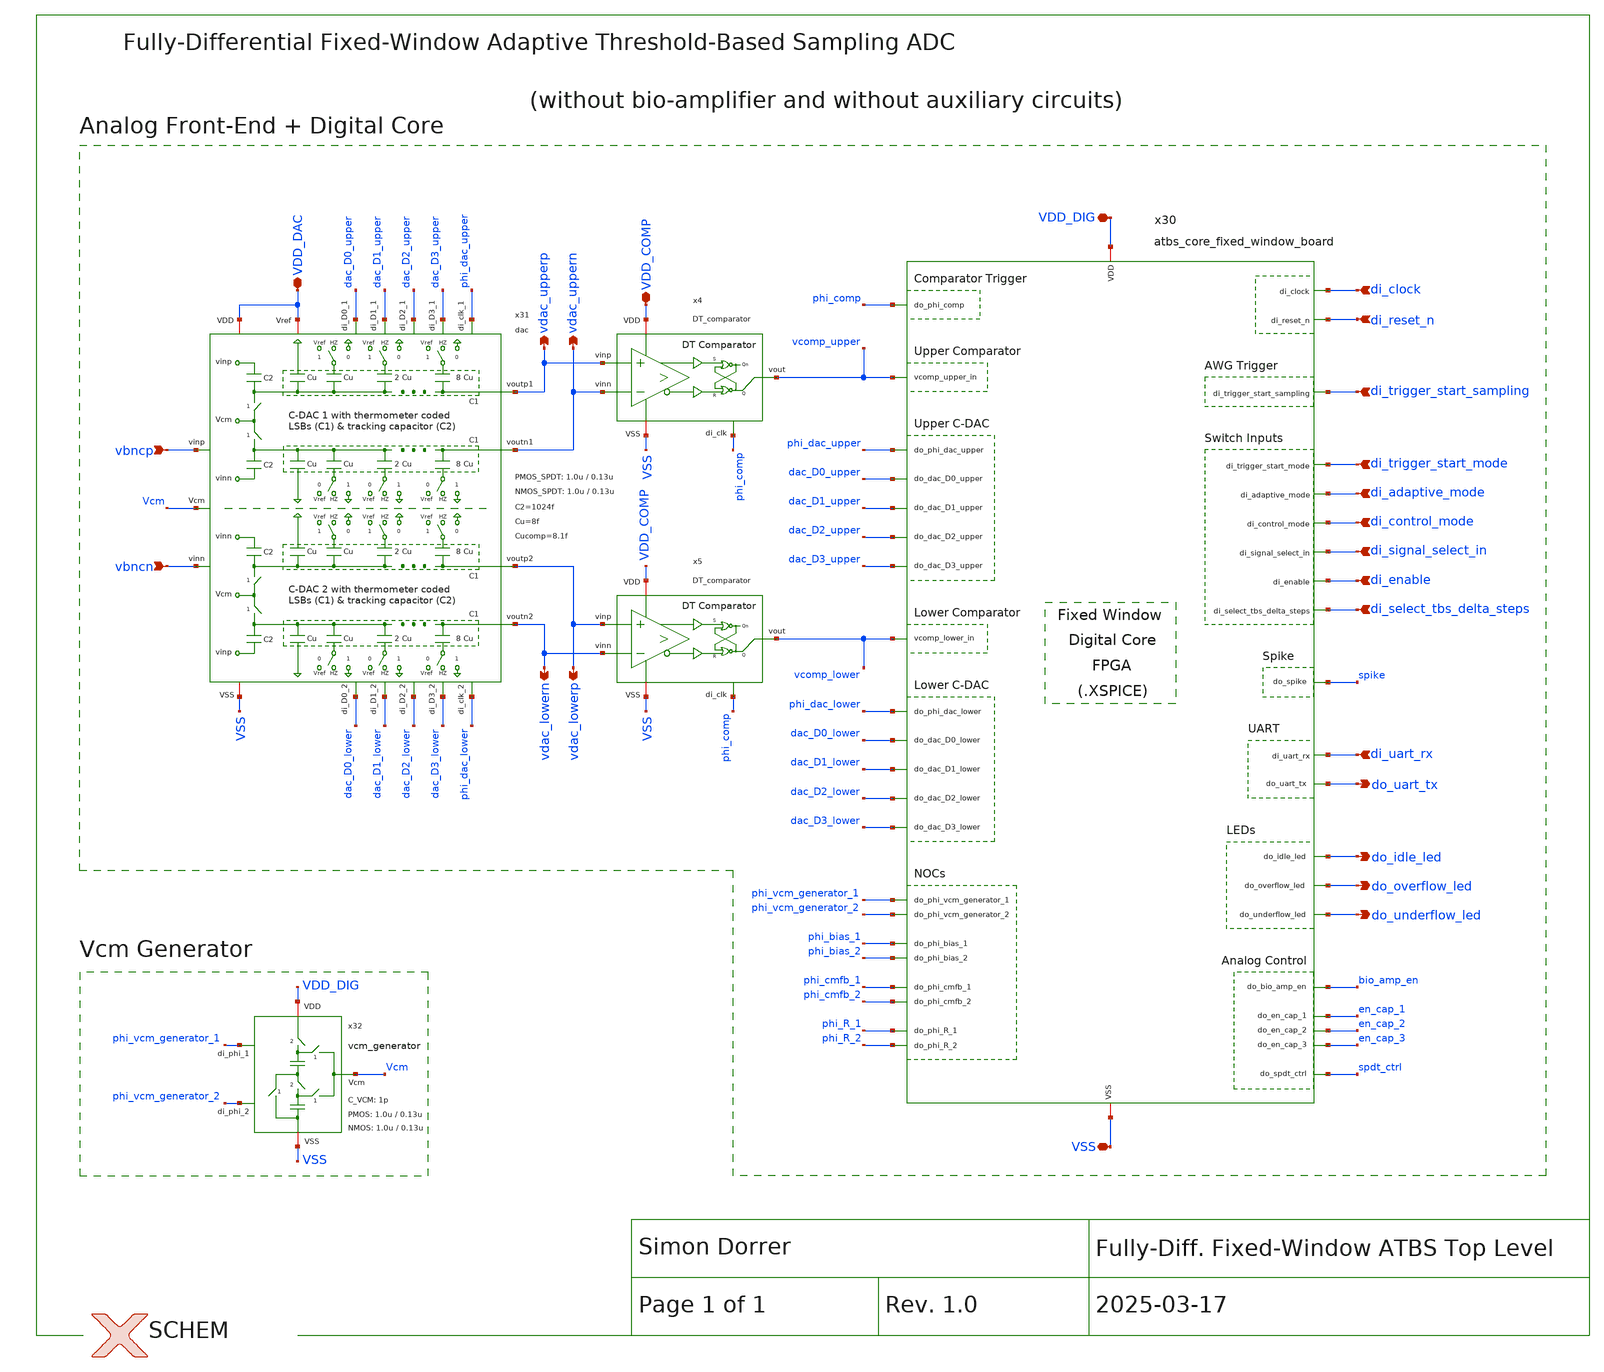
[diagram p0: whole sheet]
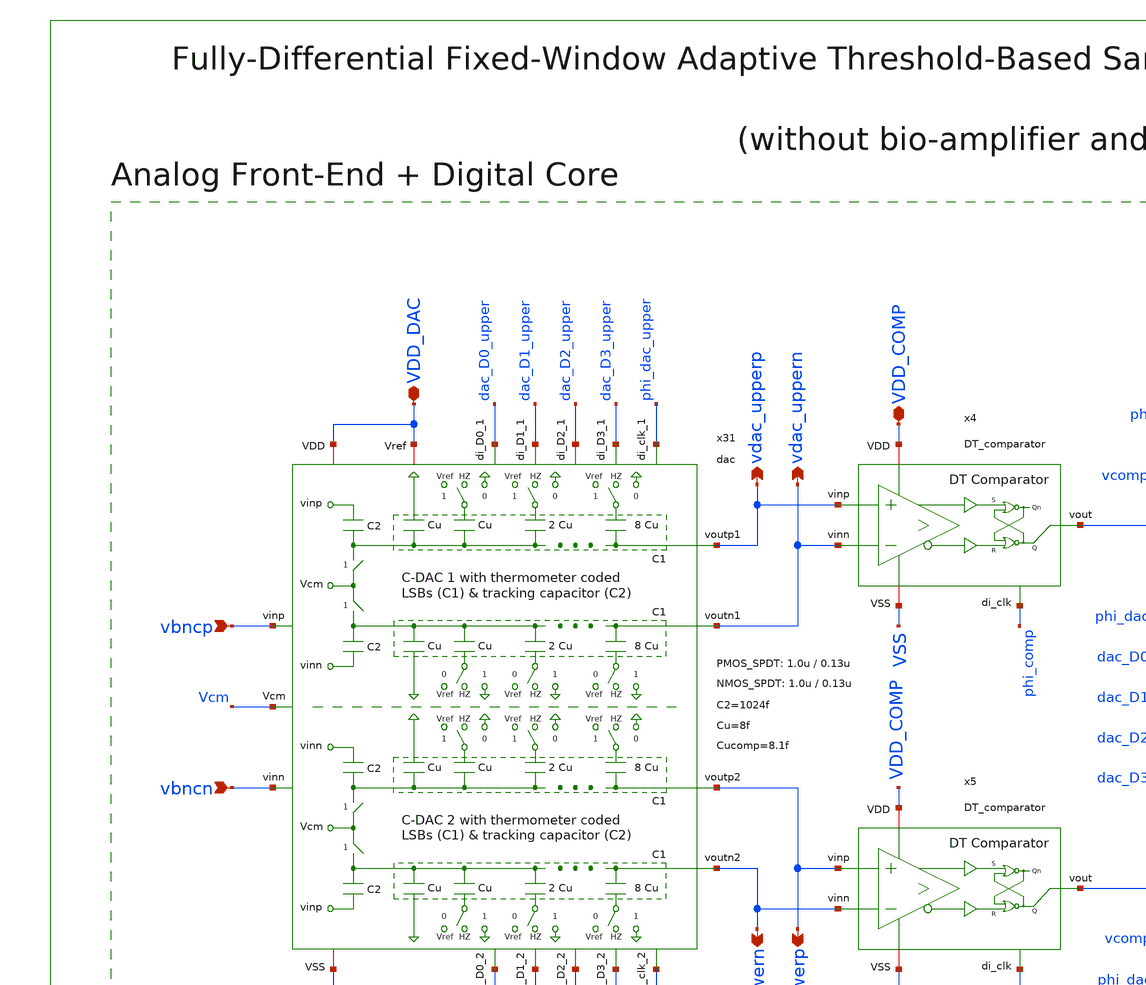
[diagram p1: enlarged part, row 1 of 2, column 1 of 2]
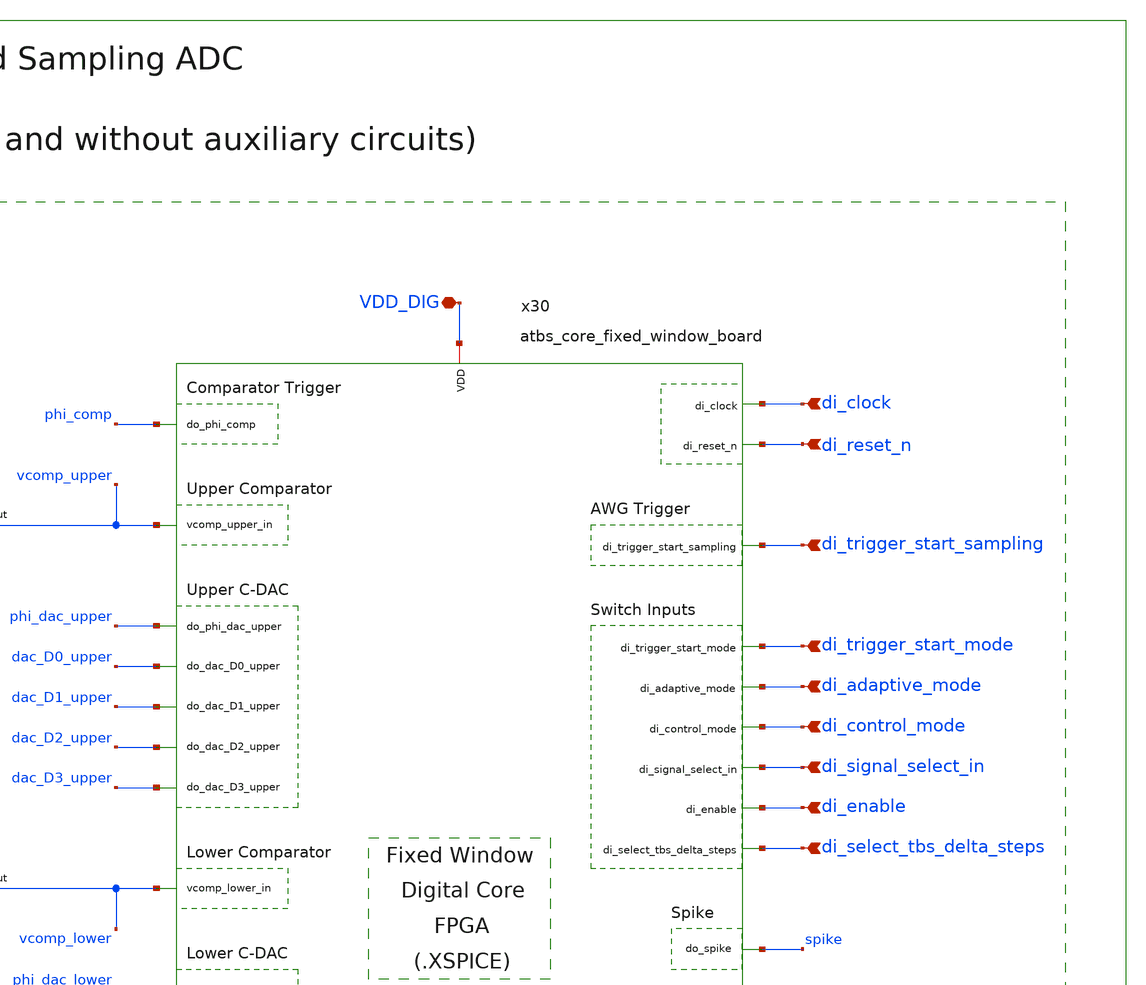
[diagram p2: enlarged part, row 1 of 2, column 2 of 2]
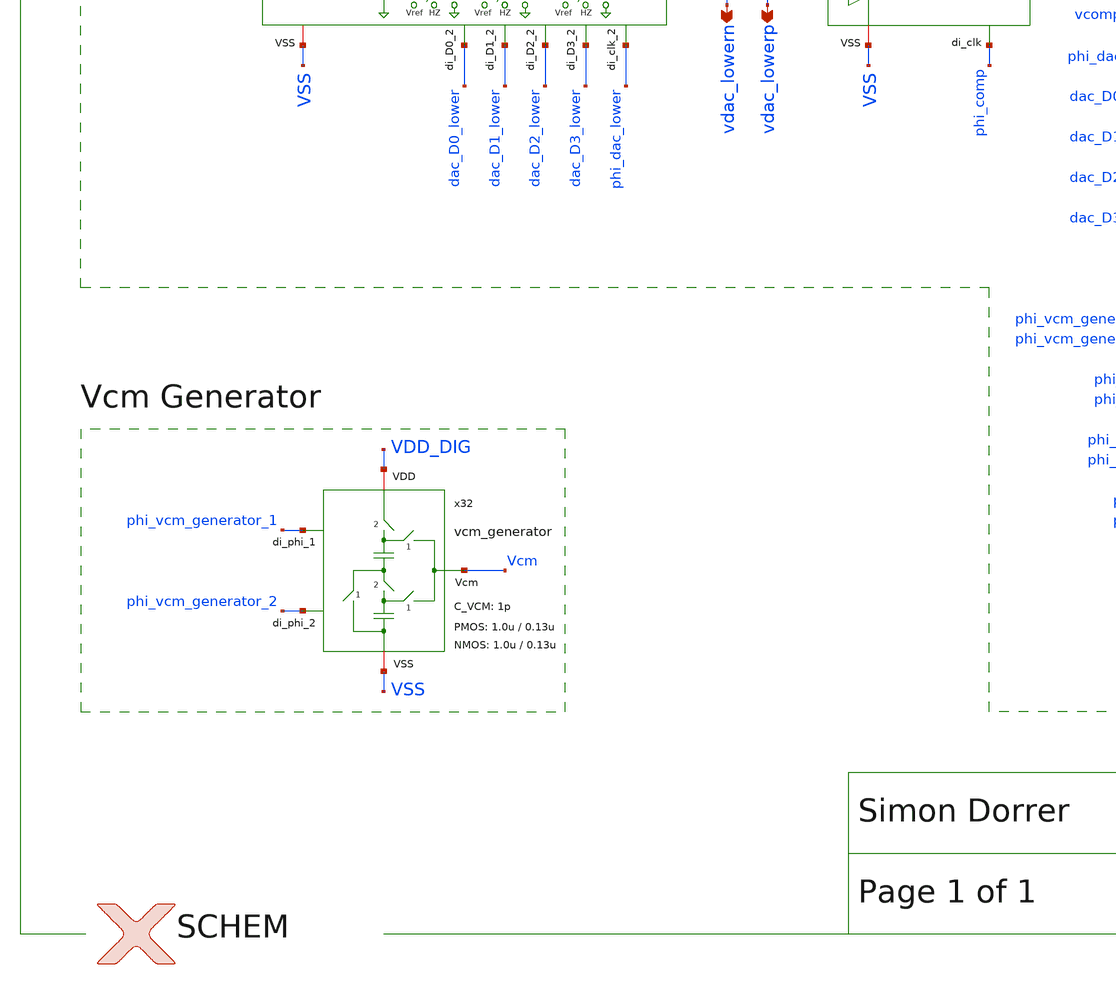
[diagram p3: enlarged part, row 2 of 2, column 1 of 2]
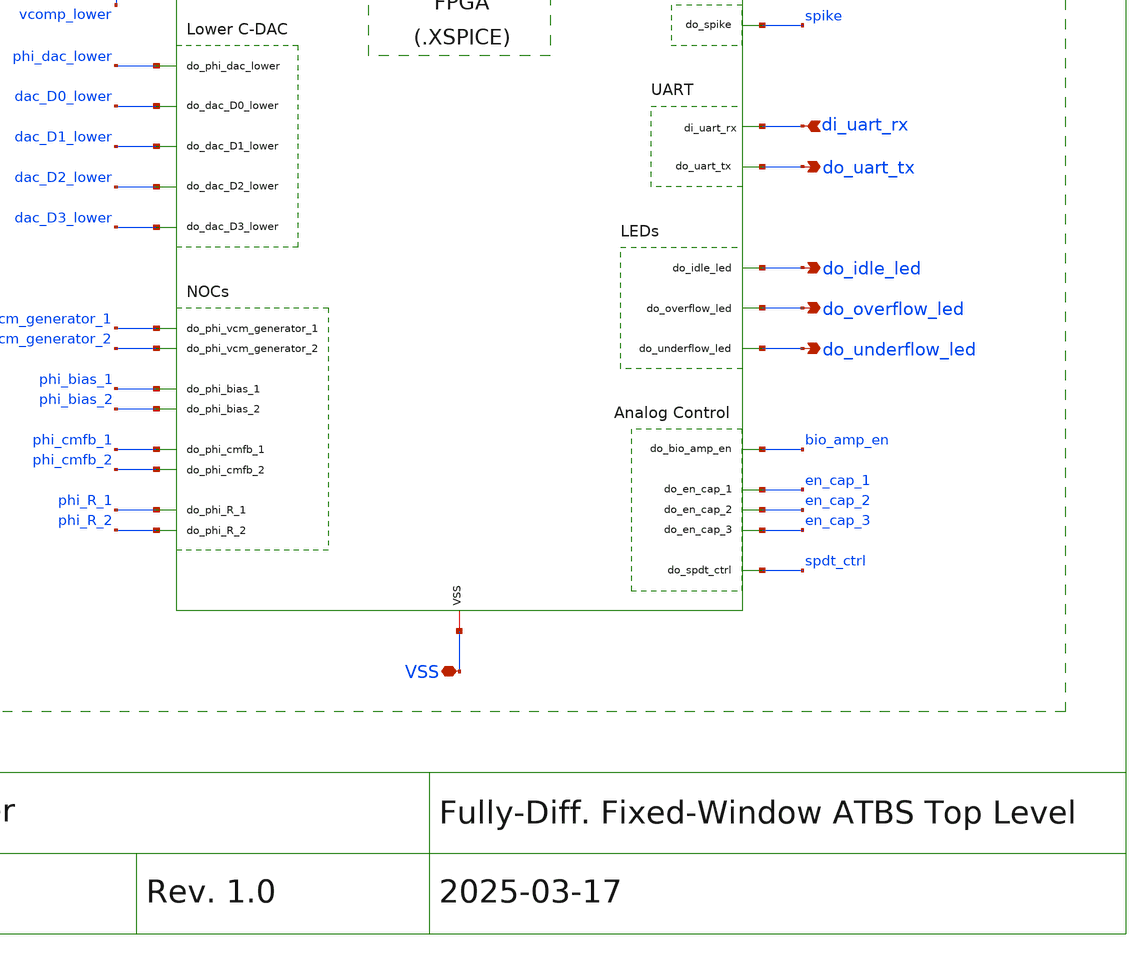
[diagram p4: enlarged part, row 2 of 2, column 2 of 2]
** sch_path: SG13G2_ATBS-ADC-main/xschem/top_level/atbs_top_fixed_window_wo_amp_aux.sch
**.subckt atbs_top_fixed_window_wo_amp_aux VDD_DIG VDD_COMP VSS di_clock di_reset_n VDD_DAC
*+ di_uart_rx do_uart_tx di_trigger_start_sampling di_trigger_start_mode di_adaptive_mode di_control_mode
*+ di_signal_select_in di_enable di_select_tbs_delta_steps do_idle_led do_overflow_led do_underflow_led vbncp vbncn
*+ vdac_upperp vdac_lowern vdac_uppern vdac_lowerp
*.iopin VDD_DIG
*.iopin VDD_COMP
*.iopin VSS
*.ipin di_clock
*.ipin di_reset_n
*.iopin VDD_DAC
*.ipin di_uart_rx
*.opin do_uart_tx
*.ipin di_trigger_start_sampling
*.ipin di_trigger_start_mode
*.ipin di_adaptive_mode
*.ipin di_control_mode
*.ipin di_signal_select_in
*.ipin di_enable
*.ipin di_select_tbs_delta_steps
*.opin do_idle_led
*.opin do_overflow_led
*.opin do_underflow_led
*.ipin vbncp
*.ipin vbncn
*.opin vdac_upperp
*.opin vdac_lowern
*.opin vdac_uppern
*.opin vdac_lowerp
x4 VDD_COMP vdac_upperp vcomp_upper vdac_uppern phi_comp VSS DT_comparator
x5 VDD_COMP vdac_lowerp vcomp_lower vdac_lowern phi_comp VSS DT_comparator
x30 VDD_DIG VSS di_adaptive_mode bio_amp_en di_clock vcomp_lower vcomp_upper di_control_mode
+ dac_D0_lower dac_D1_lower dac_D2_lower dac_D3_lower dac_D0_upper dac_D1_upper dac_D2_upper dac_D3_upper
+ di_enable do_idle_led do_overflow_led phi_bias_1 phi_bias_2 phi_cmfb_1 phi_cmfb_2 phi_comp phi_dac_lower
+ phi_dac_upper phi_R_1 phi_R_2 phi_vcm_generator_1 phi_vcm_generator_2 di_reset_n en_cap_1 en_cap_2 en_cap_3
+ spdt_ctrl di_select_tbs_delta_steps di_signal_select_in spike di_trigger_start_mode di_trigger_start_sampling
+ di_uart_rx do_uart_tx do_underflow_led atbs_core_fixed_window_board
x32 VDD_DIG phi_vcm_generator_2 phi_vcm_generator_1 Vcm VSS vcm_generator C_VCM=1p W_P_VCM=1.0u
+ L_P_VCM=0.13u W_N_VCM=1.0u L_N_VCM=0.13u
x31 VDD_DAC vbncp vdac_upperp vdac_uppern vbncn dac_D0_lower dac_D1_lower dac_D2_lower dac_D3_lower
+ VSS VDD_DAC Vcm vdac_lowerp vdac_lowern phi_dac_lower dac_D0_upper dac_D1_upper dac_D2_upper
+ dac_D3_upper phi_dac_upper dac W_P_SPDT=1.0u L_P_SPDT=0.13u W_N_SPDT=1.0u L_N_SPDT=0.13u C2=1024f Cu=8f
+ Cucomp=8.1f
**.ends

* expanding   symbol:  comparator/discrete_time/DT_comparator.sym # of pins=6
** sym_path: SG13G2_ATBS-ADC-main/xschem/comparator/discrete_time/DT_comparator.sym
** sch_path: SG13G2_ATBS-ADC-main/xschem/comparator/discrete_time/DT_comparator.sch
.subckt DT_comparator VDD vinp vout vinn di_clk VSS
*.iopin VDD
*.opin vout
*.iopin VSS
*.ipin vinp
*.ipin vinn
*.ipin di_clk
x2 VDD voutp_comp voutp_buf VSS buffer_lv W_P_INV=1.0u L_P_INV=0.13u W_N_INV=1.0u L_N_INV=0.13u
x3 VDD voutn_comp voutn_buf VSS buffer_lv W_P_INV=1.0u L_P_INV=0.13u W_N_INV=1.0u L_N_INV=0.13u
x5 VDD di_clk net1 VSS inverter_lv W_P=1.0u L_P=0.13u W_N=1.0u L_N=0.13u
* noconn #net2
x4 VDD voutp_buf net2 VSS vout voutn_buf SR_latch W_P_SR=1.0u L_P_SR=0.13u W_N_SR=1.0u L_N_SR=0.13u
x1 net1 di_clk VDD voutp_comp vinp VSS voutn_comp vinn dynamic_biasing_comparator
.ends


* expanding   symbol:  vcm_generator/vcm_generator.sym # of pins=5
** sym_path: SG13G2_ATBS-ADC-main/xschem/vcm_generator/vcm_generator.sym
** sch_path: SG13G2_ATBS-ADC-main/xschem/vcm_generator/vcm_generator.sch
.subckt vcm_generator VDD di_phi_2 di_phi_1 Vcm VSS  C_VCM=1p W_P_VCM=1.0u L_P_VCM=0.13u
+ W_N_VCM=1.0u L_N_VCM=0.13u
*.iopin VDD
*.opin Vcm
*.iopin VSS
*.ipin di_phi_1
*.ipin di_phi_2
x1 VDD di_phi_2 VSS net1 VDD di_phi_2_n transmission_gate_lv_wo_dummy W_P=W_P_VCM L_P=L_P_VCM
+ W_N=W_N_VCM L_N=L_N_VCM
x2 VDD di_phi_1 VSS Vcm net1 di_phi_1_n transmission_gate_lv_wo_dummy W_P=W_P_VCM L_P=L_P_VCM
+ W_N=W_N_VCM L_N=L_N_VCM
x3 VDD di_phi_2 VSS net3 net2 di_phi_2_n transmission_gate_lv_wo_dummy W_P=W_P_VCM L_P=L_P_VCM
+ W_N=W_N_VCM L_N=L_N_VCM
x4 VDD di_phi_1 VSS Vcm net3 di_phi_1_n transmission_gate_lv_wo_dummy W_P=W_P_VCM L_P=L_P_VCM
+ W_N=W_N_VCM L_N=L_N_VCM
x5 VDD di_phi_1 VSS VSS net2 di_phi_1_n transmission_gate_lv_wo_dummy W_P=W_P_VCM L_P=L_P_VCM
+ W_N=W_N_VCM L_N=L_N_VCM
x9 VDD di_phi_1 di_phi_1_n VSS inverter_lv W_P=W_P_VCM L_P=L_P_VCM W_N=W_N_VCM L_N=L_N_VCM
x8 VDD di_phi_2 di_phi_2_n VSS inverter_lv W_P=W_P_VCM L_P=L_P_VCM W_N=W_N_VCM L_N=L_N_VCM
C1 net1 net2 C_VCM m=1
C2 net3 VSS C_VCM m=1
.ends


* expanding   symbol:  dac/dac.sym # of pins=20
** sym_path: SG13G2_ATBS-ADC-main/xschem/dac/dac.sym
** sch_path: SG13G2_ATBS-ADC-main/xschem/dac/dac.sch
.subckt dac VDD vinp voutp1 voutn1 vinn di_D0_2 di_D1_2 di_D2_2 di_D3_2 VSS Vref Vcm voutp2 voutn2
+ di_clk_2 di_D0_1 di_D1_1 di_D2_1 di_D3_1 di_clk_1  W_P_SPDT=1.0u L_P_SPDT=0.13u W_N_SPDT=1.0u L_N_SPDT=0.13u
+ C2=1024f Cu=8f Cucomp=8.1f
*.opin voutp1
*.ipin di_D0_1
*.iopin VSS
*.iopin Vref
*.opin voutn1
*.ipin vinp
*.ipin vinn
*.ipin di_D1_1
*.ipin di_D2_1
*.ipin di_D3_1
*.opin voutp2
*.opin voutn2
*.iopin VDD
*.ipin Vcm
*.ipin di_clk_1
*.ipin di_D3_2
*.ipin di_D2_2
*.ipin di_D1_2
*.ipin di_D0_2
*.ipin di_clk_2
C2a vinp voutp1 C2 m=1
C2b vinn voutn1 C2 m=1
C1a net3 voutp1 Cucomp m=1
C1b net1 voutn1 Cucomp m=1
x2 VDD di_clk_1 VSS voutp1 Vcm clk_1_n transmission_gate_lv_wo_dummy W_P=1.0u L_P=0.13u W_N=1.0u
+ L_N=0.13u
x3 VDD di_clk_1 VSS voutn1 Vcm clk_1_n transmission_gate_lv_wo_dummy W_P=1.0u L_P=0.13u W_N=1.0u
+ L_N=0.13u
x1 VDD di_clk_1 clk_1_n VSS inverter_lv W_P=W_P_SPDT L_P=L_P_SPDT W_N=W_N_SPDT L_N=L_N_SPDT
x5 Vref VSS VSS di_D1_1 di_clk_1 VDD voutp1 unit_cell W_P_SPDT=W_P_SPDT L_P_SPDT=L_P_SPDT
+ W_N_SPDT=W_N_SPDT L_N_SPDT=L_N_SPDT Cu=2*Cu
x6 Vref VSS VSS di_D2_1 di_clk_1 VDD voutp1 unit_cell W_P_SPDT=W_P_SPDT L_P_SPDT=L_P_SPDT
+ W_N_SPDT=W_N_SPDT L_N_SPDT=L_N_SPDT Cu=4*Cu
x4 Vref VSS VSS di_D0_1 di_clk_1 VDD voutp1 unit_cell W_P_SPDT=W_P_SPDT L_P_SPDT=L_P_SPDT
+ W_N_SPDT=W_N_SPDT L_N_SPDT=L_N_SPDT Cu=Cu
x7 Vref VSS VSS di_D3_1 di_clk_1 VDD voutp1 unit_cell W_P_SPDT=W_P_SPDT L_P_SPDT=L_P_SPDT
+ W_N_SPDT=W_N_SPDT L_N_SPDT=L_N_SPDT Cu=8*Cu
x9 VSS Vref VSS di_D0_1 di_clk_1 VDD voutn1 unit_cell W_P_SPDT=W_P_SPDT L_P_SPDT=L_P_SPDT
+ W_N_SPDT=W_N_SPDT L_N_SPDT=L_N_SPDT Cu=Cu
x10 VSS Vref VSS di_D1_1 di_clk_1 VDD voutn1 unit_cell W_P_SPDT=W_P_SPDT L_P_SPDT=L_P_SPDT
+ W_N_SPDT=W_N_SPDT L_N_SPDT=L_N_SPDT Cu=2*Cu
x11 VSS Vref VSS di_D2_1 di_clk_1 VDD voutn1 unit_cell W_P_SPDT=W_P_SPDT L_P_SPDT=L_P_SPDT
+ W_N_SPDT=W_N_SPDT L_N_SPDT=L_N_SPDT Cu=4*Cu
x12 VSS Vref VSS di_D3_1 di_clk_1 VDD voutn1 unit_cell W_P_SPDT=W_P_SPDT L_P_SPDT=L_P_SPDT
+ W_N_SPDT=W_N_SPDT L_N_SPDT=L_N_SPDT Cu=8*Cu
C1 vinn voutp2 C2 m=1
C2 vinp voutn2 C2 m=1
C1c net2 voutp2 Cucomp m=1
C1d net4 voutn2 Cucomp m=1
x14 VDD di_clk_2 VSS voutp2 Vcm clk_2_n transmission_gate_lv_wo_dummy W_P=1.0u L_P=0.13u W_N=1.0u
+ L_N=0.13u
x15 VDD di_clk_2 VSS voutn2 Vcm clk_2_n transmission_gate_lv_wo_dummy W_P=1.0u L_P=0.13u W_N=1.0u
+ L_N=0.13u
x17 Vref VSS VSS di_D1_2 di_clk_2 VDD voutp2 unit_cell W_P_SPDT=W_P_SPDT L_P_SPDT=L_P_SPDT
+ W_N_SPDT=W_N_SPDT L_N_SPDT=L_N_SPDT Cu=2*Cu
x18 Vref VSS VSS di_D2_2 di_clk_2 VDD voutp2 unit_cell W_P_SPDT=W_P_SPDT L_P_SPDT=L_P_SPDT
+ W_N_SPDT=W_N_SPDT L_N_SPDT=L_N_SPDT Cu=4*Cu
x16 Vref VSS VSS di_D0_2 di_clk_2 VDD voutp2 unit_cell W_P_SPDT=W_P_SPDT L_P_SPDT=L_P_SPDT
+ W_N_SPDT=W_N_SPDT L_N_SPDT=L_N_SPDT Cu=Cu
x19 Vref VSS VSS di_D3_2 di_clk_2 VDD voutp2 unit_cell W_P_SPDT=W_P_SPDT L_P_SPDT=L_P_SPDT
+ W_N_SPDT=W_N_SPDT L_N_SPDT=L_N_SPDT Cu=8*Cu
x21 VSS Vref VSS di_D0_2 di_clk_2 VDD voutn2 unit_cell W_P_SPDT=W_P_SPDT L_P_SPDT=L_P_SPDT
+ W_N_SPDT=W_N_SPDT L_N_SPDT=L_N_SPDT Cu=Cu
x22 VSS Vref VSS di_D1_2 di_clk_2 VDD voutn2 unit_cell W_P_SPDT=W_P_SPDT L_P_SPDT=L_P_SPDT
+ W_N_SPDT=W_N_SPDT L_N_SPDT=L_N_SPDT Cu=2*Cu
x23 VSS Vref VSS di_D2_2 di_clk_2 VDD voutn2 unit_cell W_P_SPDT=W_P_SPDT L_P_SPDT=L_P_SPDT
+ W_N_SPDT=W_N_SPDT L_N_SPDT=L_N_SPDT Cu=4*Cu
x24 VSS Vref VSS di_D3_2 di_clk_2 VDD voutn2 unit_cell W_P_SPDT=W_P_SPDT L_P_SPDT=L_P_SPDT
+ W_N_SPDT=W_N_SPDT L_N_SPDT=L_N_SPDT Cu=8*Cu
x8 VDD di_clk_1 VSS net3 VSS Vref spdt_switch W_P_TG=W_P_SPDT L_P_TG=L_P_SPDT W_N_TG=W_N_SPDT
+ L_N_TG=L_N_SPDT
x13 VDD di_clk_1 VSS net1 Vref VSS spdt_switch W_P_TG=W_P_SPDT L_P_TG=L_P_SPDT W_N_TG=W_N_SPDT
+ L_N_TG=L_N_SPDT
x20 VDD di_clk_2 VSS net2 VSS Vref spdt_switch W_P_TG=W_P_SPDT L_P_TG=L_P_SPDT W_N_TG=W_N_SPDT
+ L_N_TG=L_N_SPDT
x25 VDD di_clk_2 VSS net4 Vref VSS spdt_switch W_P_TG=W_P_SPDT L_P_TG=L_P_SPDT W_N_TG=W_N_SPDT
+ L_N_TG=L_N_SPDT
x26 VDD di_clk_2 clk_2_n VSS inverter_lv W_P=W_P_SPDT L_P=L_P_SPDT W_N=W_N_SPDT L_N=L_N_SPDT
.ends


* expanding   symbol:  buffer/buffer_lv.sym # of pins=4
** sym_path: SG13G2_ATBS-ADC-main/xschem/buffer/buffer_lv.sym
** sch_path: SG13G2_ATBS-ADC-main/xschem/buffer/buffer_lv.sch
.subckt buffer_lv VDD vin vout VSS  W_P_INV=3.0u L_P_INV=0.13u W_N_INV=1.0u L_N_INV=0.13u
*.ipin vin
*.iopin VDD
*.iopin VSS
*.opin vout
x1 VDD vin net1 VSS inverter_lv W_P=W_P_INV L_P=L_P_INV W_N=W_N_INV L_N=L_N_INV
x2 VDD net1 vout VSS inverter_lv W_P=W_P_INV L_P=L_P_INV W_N=W_N_INV L_N=L_N_INV
.ends


* expanding   symbol:  inverter/inverter_lv.sym # of pins=4
** sym_path: SG13G2_ATBS-ADC-main/xschem/inverter/inverter_lv.sym
** sch_path: SG13G2_ATBS-ADC-main/xschem/inverter/inverter_lv.sch
.subckt inverter_lv VDD vin vout VSS  W_P=3.0u L_P=0.13u W_N=1.0u L_N=0.13u
*.ipin vin
*.iopin VDD
*.iopin VSS
*.opin vout
XM1 vout vin VDD VDD sg13_lv_pmos w=W_P l=L_P ng=1 m=1 mm_ok=1
XM2 vout vin VSS VSS sg13_lv_nmos w=W_N l=L_N ng=1 m=1 mm_ok=1
.ends


* expanding   symbol:  comparator/SR_latch/SR_latch.sym # of pins=6
** sym_path: SG13G2_ATBS-ADC-main/xschem/comparator/SR_latch/SR_latch.sym
** sch_path: SG13G2_ATBS-ADC-main/xschem/comparator/SR_latch/SR_latch.sch
.subckt SR_latch VDD S Qn VSS Q R  W_P_SR=1.0u L_P_SR=0.13u W_N_SR=1.0u L_N_SR=0.13u
*.iopin VDD
*.opin Q
*.iopin VSS
*.ipin S
*.ipin R
*.opin Qn
x1 VDD Q R Qn VSS NOR_gate W_P=W_P_SR L_P=L_P_SR W_N=W_N_SR L_N=L_N_SR
x2 VDD Qn Q S VSS NOR_gate W_P=W_P_SR L_P=L_P_SR W_N=W_N_SR L_N=L_N_SR
.ends


* expanding   symbol:  comparator/discrete_time/Dynamic-biasing/dynamic_biasing_comparator.sym # of
*+ pins=8
** sym_path: SG13G2_ATBS-ADC-main/xschem/comparator/discrete_time/Dynamic-biasing/dynamic_biasing_comparator.sym
** sch_path: SG13G2_ATBS-ADC-main/xschem/comparator/discrete_time/Dynamic-biasing/dynamic_biasing_comparator.sch
.subckt dynamic_biasing_comparator di_clk_n di_clk VDD voutp vinp VSS voutn vinn
*.iopin VDD
*.opin voutp
*.opin voutn
*.ipin di_clk_n
*.iopin VSS
*.ipin vinp
*.ipin vinn
*.ipin di_clk
XM3a vs di_clk vctail VSS sg13_lv_nmos w=1.0u l=0.13u ng=1 m=1 mm_ok=1
XM12 voutp di_clk_n VSS VSS sg13_lv_nmos w=1.0u l=0.13u ng=1 m=1 mm_ok=1
XM8 net1 voutn VDD VDD sg13_lv_pmos w=2.0u l=0.13u ng=2 m=1 mm_ok=1
XM10 voutp voutn VSS VSS sg13_lv_nmos w=1.0u l=0.13u ng=1 m=1 mm_ok=1
XM11 voutn voutp VSS VSS sg13_lv_nmos w=1.0u l=0.13u ng=1 m=1 mm_ok=1
XM13 voutn di_clk_n VSS VSS sg13_lv_nmos w=1.0u l=0.13u ng=1 m=1 mm_ok=1
CPn vcpn VSS 300f m=1
CPp vcpp VSS 300f m=1
XM9 net2 voutp VDD VDD sg13_lv_pmos w=2.0u l=0.13u ng=2 m=1 mm_ok=1
XM6 voutp vcpn net1 VDD sg13_lv_pmos w=2.0u l=0.13u ng=2 m=1 mm_ok=1
XM7 voutn vcpp net2 VDD sg13_lv_pmos w=2.0u l=0.13u ng=2 m=1 mm_ok=1
CTAIL vctail VSS 600f m=1
XM3b vctail di_clk_n VSS VSS sg13_lv_nmos w=1.0u l=0.13u ng=1 m=1 mm_ok=1
XM1 vcpn vinp vs VSS sg13_lv_nmos w=1.0u l=0.13u ng=1 m=1 mm_ok=1
XM2 vcpp vinn vs VSS sg13_lv_nmos w=1.0u l=0.13u ng=1 m=1 mm_ok=1
XM4 vcpn di_clk VDD VDD sg13_lv_pmos w=1.0u l=0.13u ng=1 m=1 mm_ok=1
XM5 vcpp di_clk VDD VDD sg13_lv_pmos w=1.0u l=0.13u ng=1 m=1 mm_ok=1
.ends


* expanding   symbol:  transmission_gate/transmission_gate_lv_wo_dummy.sym # of pins=6
** sym_path: SG13G2_ATBS-ADC-main/xschem/transmission_gate/transmission_gate_lv_wo_dummy.sym
** sch_path: SG13G2_ATBS-ADC-main/xschem/transmission_gate/transmission_gate_lv_wo_dummy.sch
.subckt transmission_gate_lv_wo_dummy VDD di_tg_ctrl VSS v_b v_a di_tg_ctrl_n  W_P=1.0u L_P=0.13u
+ W_N=1.0u L_N=0.13u
*.iopin v_a
*.iopin v_b
*.iopin VDD
*.iopin VSS
*.ipin di_tg_ctrl
*.ipin di_tg_ctrl_n
XM1 v_a di_tg_ctrl v_b VSS sg13_lv_nmos w=W_N l=L_N ng=1 m=1 mm_ok=1
XM2 v_a di_tg_ctrl_n v_b VDD sg13_lv_pmos w=W_P l=L_P ng=1 m=1 mm_ok=1
.ends


* expanding   symbol:  dac/unit_cell.sym # of pins=7
** sym_path: SG13G2_ATBS-ADC-main/xschem/dac/unit_cell.sym
** sch_path: SG13G2_ATBS-ADC-main/xschem/dac/unit_cell.sch
.subckt unit_cell v1 v0 VSS di_cell_en di_clk VDD vtop  W_P_SPDT=1.0u L_P_SPDT=0.13u W_N_SPDT=1.0u
+ L_N_SPDT=0.13u Cu=8f
*.ipin di_cell_en
*.iopin VSS
*.iopin v0
*.iopin VDD
*.ipin di_clk
*.iopin v1
*.iopin vtop
x1 VDD di_clk VSS net1 v0 v1 di_cell_en_n spdt_hz_switch W_P_TG=W_P_SPDT L_P_TG=L_P_SPDT
+ W_N_TG=W_N_SPDT L_N_TG=L_N_SPDT
C1 net1 vtop Cu m=1
x3 VDD di_cell_en di_cell_en_n VSS inverter_lv W_P=W_P_SPDT L_P=W_P_SPDT W_N=W_N_SPDT L_N=W_N_SPDT
.ends


* expanding   symbol:  spdt_switch/spdt_switch.sym # of pins=6
** sym_path: SG13G2_ATBS-ADC-main/xschem/spdt_switch/spdt_switch.sym
** sch_path: SG13G2_ATBS-ADC-main/xschem/spdt_switch/spdt_switch.sch
.subckt spdt_switch VDD di_spdt_ctrl VSS v_c v_b v_a  W_P_TG=3.0u L_P_TG=0.13u W_N_TG=1.0u
+ L_N_TG=0.13u
*.iopin v_a
*.iopin v_b
*.iopin v_c
*.iopin VDD
*.iopin VSS
*.ipin di_spdt_ctrl
x1 VDD di_spdt_ctrl VSS v_c v_a di_spdt_ctrl_n transmission_gate_lv_wo_dummy W_P=W_P_TG L_P=L_P_TG
+ W_N=W_N_TG L_N=L_N_TG
x2 VDD di_spdt_ctrl_n VSS v_b v_c di_spdt_ctrl transmission_gate_lv_wo_dummy W_P=W_P_TG L_P=L_P_TG
+ W_N=W_N_TG L_N=L_N_TG
x8 VDD di_spdt_ctrl di_spdt_ctrl_n VSS inverter_lv W_P=W_P_TG L_P=L_P_TG W_N=W_N_TG L_N=L_N_TG
.ends


* expanding   symbol:  comparator/NOR_gate/NOR_gate.sym # of pins=5
** sym_path: SG13G2_ATBS-ADC-main/xschem/comparator/NOR_gate/NOR_gate.sym
** sch_path: SG13G2_ATBS-ADC-main/xschem/comparator/NOR_gate/NOR_gate.sch
.subckt NOR_gate VDD C A B VSS  W_P=1.0u L_P=0.13u W_N=0.5u L_N=0.13u
*.iopin VDD
*.opin C
*.iopin VSS
*.ipin A
*.ipin B
XM1 C A VSS VSS sg13_lv_nmos w=W_N l=L_N ng=1 m=1 mm_ok=1
XM2 C B VSS VSS sg13_lv_nmos w=W_N l=L_N ng=1 m=1 mm_ok=1
XM3 C B net1 VDD sg13_lv_pmos w=W_P l=L_P ng=1 m=1 mm_ok=1
XM4 net1 A VDD VDD sg13_lv_pmos w=W_P l=L_P ng=1 m=1 mm_ok=1
XM5 C A net2 VDD sg13_lv_pmos w=W_P l=L_P ng=1 m=1 mm_ok=1
XM6 net2 B VDD VDD sg13_lv_pmos w=W_P l=L_P ng=1 m=1 mm_ok=1
.ends


* expanding   symbol:  spdt_switch/spdt_hz_switch.sym # of pins=7
** sym_path: SG13G2_ATBS-ADC-main/xschem/spdt_switch/spdt_hz_switch.sym
** sch_path: SG13G2_ATBS-ADC-main/xschem/spdt_switch/spdt_hz_switch.sch
.subckt spdt_hz_switch VDD di_spdt_ctrl VSS v_c v_b v_a di_spdt_hz  W_P_TG=3.0u L_P_TG=0.13u
+ W_N_TG=1.0u L_N_TG=0.13u
*.iopin v_a
*.iopin v_b
*.iopin v_c
*.iopin VDD
*.iopin VSS
*.ipin di_spdt_ctrl
*.ipin di_spdt_hz
x1 VDD di_spdt_ctrl VSS net1 v_a di_spdt_ctrl_n transmission_gate_lv_wo_dummy W_P=W_P_TG L_P=L_P_TG
+ W_N=W_N_TG L_N=L_N_TG
x2 VDD di_spdt_ctrl_n VSS v_b net1 di_spdt_ctrl transmission_gate_lv_wo_dummy W_P=W_P_TG L_P=L_P_TG
+ W_N=W_N_TG L_N=L_N_TG
x8 VDD di_spdt_ctrl di_spdt_ctrl_n VSS inverter_lv W_P=W_P_TG L_P=L_P_TG W_N=W_N_TG L_N=L_N_TG
x3 VDD di_spdt_hz di_spdt_hz_n VSS inverter_lv W_P=W_P_TG L_P=L_P_TG W_N=W_N_TG L_N=L_N_TG
x4 VDD di_spdt_hz_n VSS v_c net1 di_spdt_hz transmission_gate_lv_wo_dummy W_P=W_P_TG L_P=L_P_TG
+ W_N=W_N_TG L_N=L_N_TG
.ends

.end
